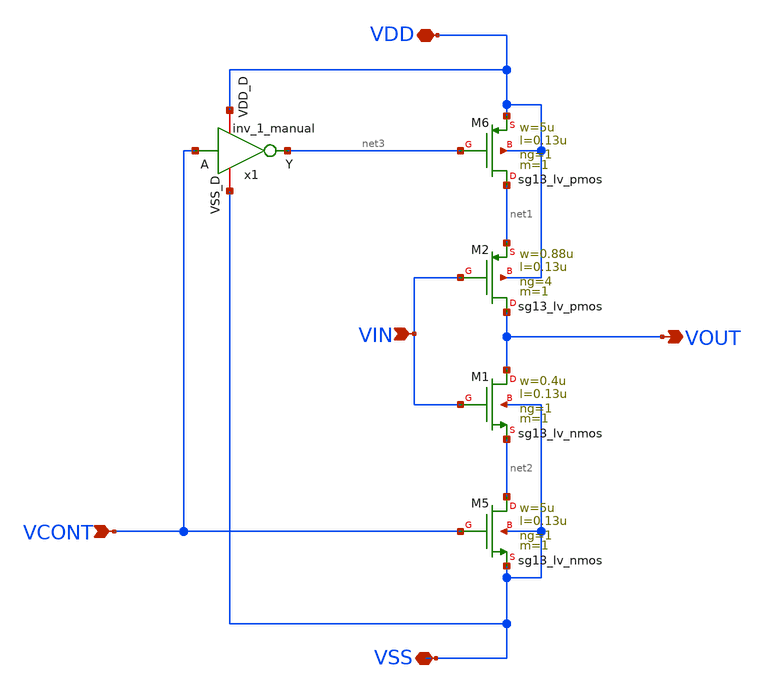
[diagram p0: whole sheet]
** sch_path: variable_delay.sch
**.subckt variable_delay VSS VDD VIN VOUT VCONT
*.iopin VSS
*.iopin VDD
*.ipin VIN
*.opin VOUT
*.ipin VCONT
XM5 net2 VCONT VSS VSS sg13_lv_nmos w=5u l=0.13u ng=1 m=1 mm_ok=1
XM6 net1 net3 VDD VDD sg13_lv_pmos w=5u l=0.13u ng=1 m=1 mm_ok=1
XM2 VOUT VIN net1 VDD sg13_lv_pmos w=0.88u l=0.13u ng=4 m=1 mm_ok=1
XM1 VOUT VIN net2 VSS sg13_lv_nmos w=0.4u l=0.13u ng=1 m=1 mm_ok=1
x1 VDD VCONT net3 VSS inv_1_manual
**.ends
.end
